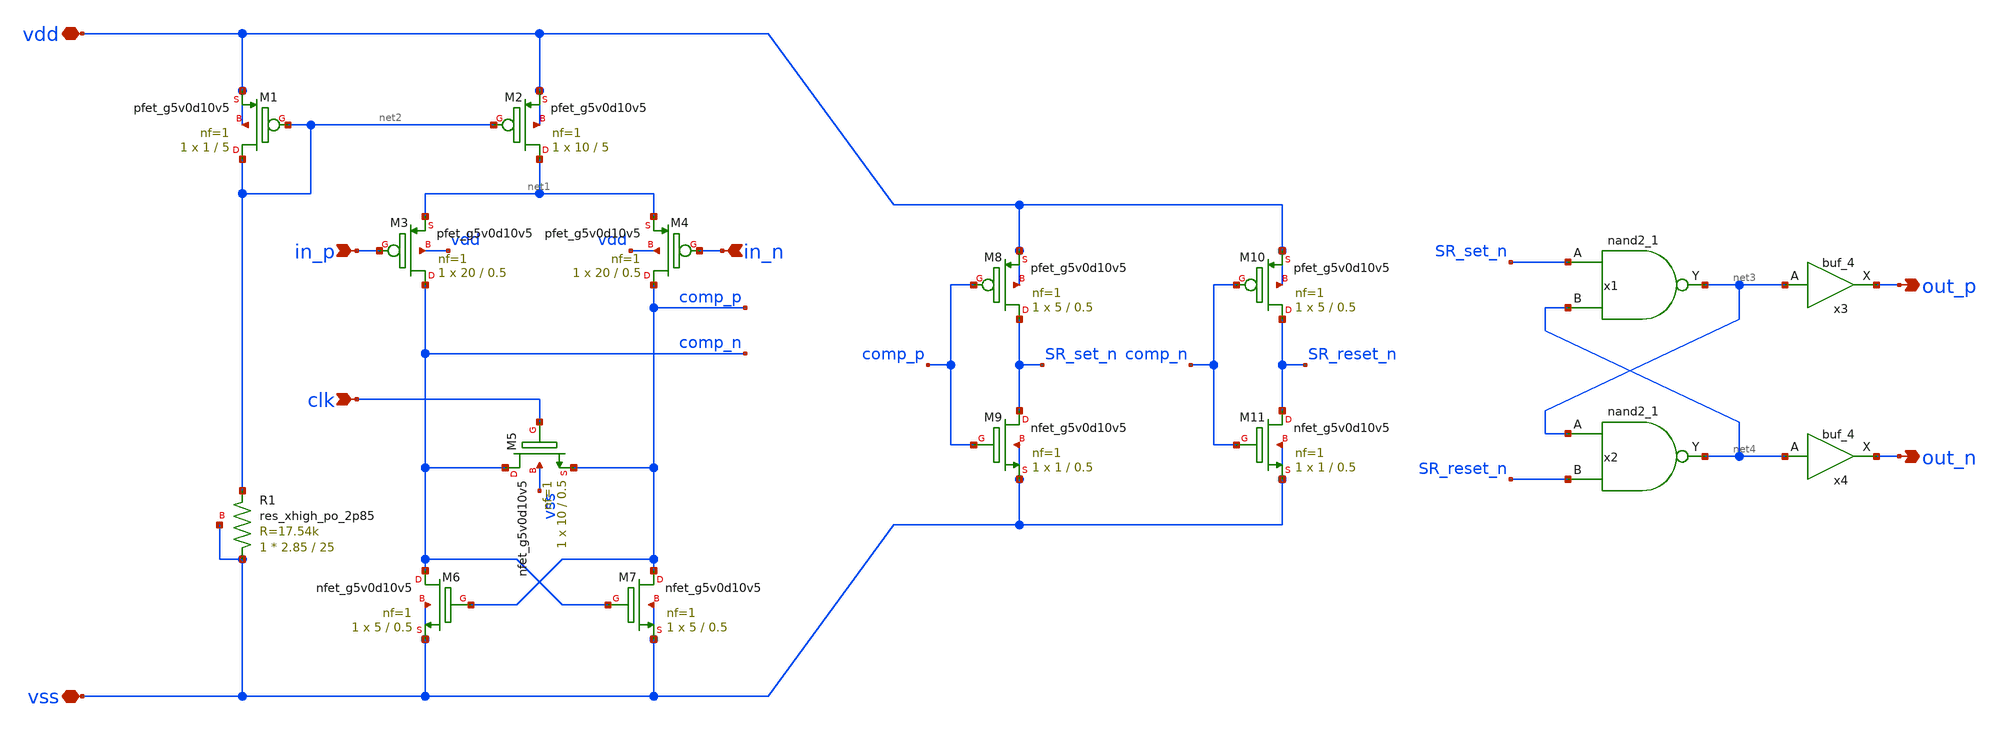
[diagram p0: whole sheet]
** sch_path: custom_gds/tt_um_tt08_aicd_playground/dependencies/sky130_leo_ip__comparator/xschem/sky130_leo_ip__comparator.sch
**.subckt sky130_leo_ip__comparator out_n in_p in_n vdd vss clk out_p
*.opin out_n
*.ipin in_p
*.ipin in_n
*.iopin vdd
*.iopin vss
*.ipin clk
*.opin out_p
XR1 vss net2 vss sky130_fd_pr__res_xhigh_po_2p85 L=25 mult=1 m=1
XM7 comp_p comp_n vss vss sky130_fd_pr__nfet_g5v0d10v5 L=0.5 W=5 nf=1 ad='int((nf+1)/2) * W/nf * 0.29'
+ as='int((nf+2)/2) * W/nf * 0.29' pd='2*int((nf+1)/2) * (W/nf + 0.29)' ps='2*int((nf+2)/2) * (W/nf + 0.29)'
+ nrd='0.29 / W' nrs='0.29 / W' sa=0 sb=0 sd=0 mult=1 m=1
XM1 net2 net2 vdd vdd sky130_fd_pr__pfet_g5v0d10v5 L=5 W=1 nf=1 ad='int((nf+1)/2) * W/nf * 0.29' as='int((nf+2)/2) * W/nf * 0.29'
+ pd='2*int((nf+1)/2) * (W/nf + 0.29)' ps='2*int((nf+2)/2) * (W/nf + 0.29)' nrd='0.29 / W' nrs='0.29 / W'
+ sa=0 sb=0 sd=0 mult=1 m=1
XM6 comp_n comp_p vss vss sky130_fd_pr__nfet_g5v0d10v5 L=0.5 W=5 nf=1 ad='int((nf+1)/2) * W/nf * 0.29'
+ as='int((nf+2)/2) * W/nf * 0.29' pd='2*int((nf+1)/2) * (W/nf + 0.29)' ps='2*int((nf+2)/2) * (W/nf + 0.29)'
+ nrd='0.29 / W' nrs='0.29 / W' sa=0 sb=0 sd=0 mult=1 m=1
XM2 net1 net2 vdd vdd sky130_fd_pr__pfet_g5v0d10v5 L=5 W=10 nf=1 ad='int((nf+1)/2) * W/nf * 0.29' as='int((nf+2)/2) * W/nf * 0.29'
+ pd='2*int((nf+1)/2) * (W/nf + 0.29)' ps='2*int((nf+2)/2) * (W/nf + 0.29)' nrd='0.29 / W' nrs='0.29 / W'
+ sa=0 sb=0 sd=0 mult=1 m=1
XM4 comp_p in_n net1 vdd sky130_fd_pr__pfet_g5v0d10v5 L=0.5 W=20 nf=1 ad='int((nf+1)/2) * W/nf * 0.29'
+ as='int((nf+2)/2) * W/nf * 0.29' pd='2*int((nf+1)/2) * (W/nf + 0.29)' ps='2*int((nf+2)/2) * (W/nf + 0.29)'
+ nrd='0.29 / W' nrs='0.29 / W' sa=0 sb=0 sd=0 mult=1 m=1
XM3 comp_n in_p net1 vdd sky130_fd_pr__pfet_g5v0d10v5 L=0.5 W=20 nf=1 ad='int((nf+1)/2) * W/nf * 0.29'
+ as='int((nf+2)/2) * W/nf * 0.29' pd='2*int((nf+1)/2) * (W/nf + 0.29)' ps='2*int((nf+2)/2) * (W/nf + 0.29)'
+ nrd='0.29 / W' nrs='0.29 / W' sa=0 sb=0 sd=0 mult=1 m=1
XM5 comp_n clk comp_p vss sky130_fd_pr__nfet_g5v0d10v5 L=0.5 W=10 nf=1 ad='int((nf+1)/2) * W/nf * 0.29'
+ as='int((nf+2)/2) * W/nf * 0.29' pd='2*int((nf+1)/2) * (W/nf + 0.29)' ps='2*int((nf+2)/2) * (W/nf + 0.29)'
+ nrd='0.29 / W' nrs='0.29 / W' sa=0 sb=0 sd=0 mult=1 m=1
x1 SR_set_n net4 VSS VSS VDD VDD net3 sky130_fd_sc_hvl__nand2_1
x2 net3 SR_reset_n VSS VSS VDD VDD net4 sky130_fd_sc_hvl__nand2_1
XM8 SR_set_n comp_p vdd vdd sky130_fd_pr__pfet_g5v0d10v5 L=0.5 W=5 nf=1 ad='int((nf+1)/2) * W/nf * 0.29'
+ as='int((nf+2)/2) * W/nf * 0.29' pd='2*int((nf+1)/2) * (W/nf + 0.29)' ps='2*int((nf+2)/2) * (W/nf + 0.29)'
+ nrd='0.29 / W' nrs='0.29 / W' sa=0 sb=0 sd=0 mult=1 m=1
XM9 SR_set_n comp_p vss vss sky130_fd_pr__nfet_g5v0d10v5 L=0.5 W=1 nf=1 ad='int((nf+1)/2) * W/nf * 0.29'
+ as='int((nf+2)/2) * W/nf * 0.29' pd='2*int((nf+1)/2) * (W/nf + 0.29)' ps='2*int((nf+2)/2) * (W/nf + 0.29)'
+ nrd='0.29 / W' nrs='0.29 / W' sa=0 sb=0 sd=0 mult=1 m=1
XM10 SR_reset_n comp_n vdd vdd sky130_fd_pr__pfet_g5v0d10v5 L=0.5 W=5 nf=1 ad='int((nf+1)/2) * W/nf * 0.29'
+ as='int((nf+2)/2) * W/nf * 0.29' pd='2*int((nf+1)/2) * (W/nf + 0.29)' ps='2*int((nf+2)/2) * (W/nf + 0.29)'
+ nrd='0.29 / W' nrs='0.29 / W' sa=0 sb=0 sd=0 mult=1 m=1
XM11 SR_reset_n comp_n vss vss sky130_fd_pr__nfet_g5v0d10v5 L=0.5 W=1 nf=1 ad='int((nf+1)/2) * W/nf * 0.29'
+ as='int((nf+2)/2) * W/nf * 0.29' pd='2*int((nf+1)/2) * (W/nf + 0.29)' ps='2*int((nf+2)/2) * (W/nf + 0.29)'
+ nrd='0.29 / W' nrs='0.29 / W' sa=0 sb=0 sd=0 mult=1 m=1
x3 net3 VSS VSS VDD VDD out_p sky130_fd_sc_hvl__buf_4
x4 net4 VSS VSS VDD VDD out_n sky130_fd_sc_hvl__buf_4
**.ends
.end
